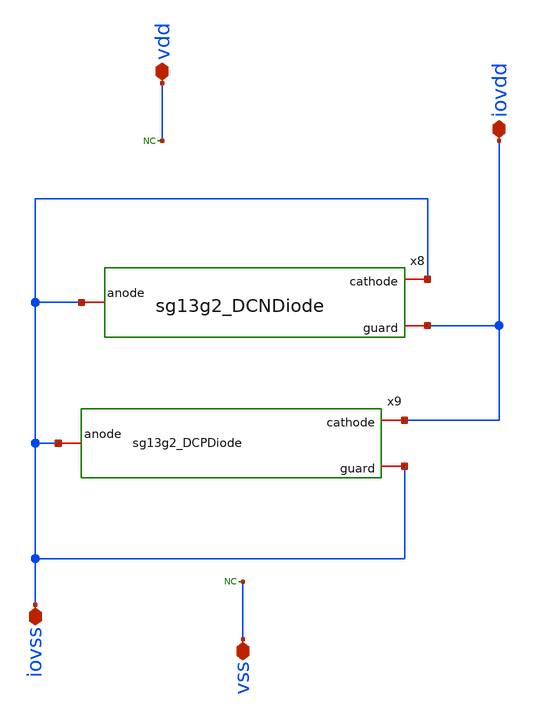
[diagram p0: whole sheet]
** sch_path: ihp-sg13g2/libs.ref/sg13g2_io/xschem/sg13g2_IOPadIOVss.sch
**.subckt sg13g2_IOPadIOVss iovss iovdd vdd vss
*.iopin iovss
*.iopin iovdd
*.iopin vdd
*.iopin vss
x8 iovss iovss iovdd sg13g2_DCNDiode
x9 iovdd iovss iovss sg13g2_DCPDiode
* noconn vdd
* noconn vss
**.ends

* expanding   symbol:  sg13g2_DCNDiode.sym # of pins=3
** sym_path: sg13g2_DCNDiode.sym
** sch_path: sg13g2_DCNDiode.sch
.subckt sg13g2_DCNDiode cathode anode guard
*.iopin cathode
*.iopin anode
*.iopin guard
XD1 anode cathode dantenna l=1.26u w=27.78u
XD2 anode cathode dantenna l=1.26u w=27.78u
.ends


* expanding   symbol:  sg13g2_DCPDiode.sym # of pins=3
** sym_path: sg13g2_DCPDiode.sym
** sch_path: sg13g2_DCPDiode.sch
.subckt sg13g2_DCPDiode cathode anode guard
*.iopin cathode
*.iopin anode
*.iopin guard
XD1 anode cathode dpantenna l=1.26u w=27.78u
XD2 anode cathode dpantenna l=1.26u w=27.78u
.ends

.end
